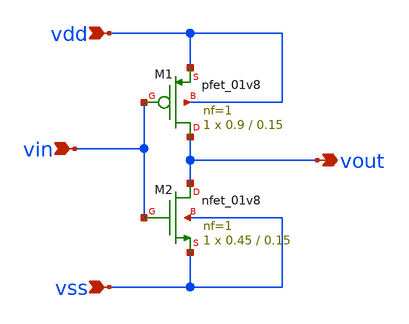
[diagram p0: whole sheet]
** sch_path: track_vlsi/lado/sch/inverter.sch
**.subckt inverter vout vdd vin vss
*.opin vout
*.ipin vdd
*.ipin vin
*.ipin vss
XM1 vout vin vdd vdd sky130_fd_pr__pfet_01v8 L=0.15 W=0.9 nf=1 ad='int((nf+1)/2) * W/nf * 0.29' as='int((nf+2)/2) * W/nf * 0.29'
+ pd='2*int((nf+1)/2) * (W/nf + 0.29)' ps='2*int((nf+2)/2) * (W/nf + 0.29)' nrd='0.29 / W' nrs='0.29 / W'
+ sa=0 sb=0 sd=0 mult=1 m=1
XM2 vout vin vss vss sky130_fd_pr__nfet_01v8 L=0.15 W=0.45 nf=1 ad='int((nf+1)/2) * W/nf * 0.29' as='int((nf+2)/2) * W/nf * 0.29'
+ pd='2*int((nf+1)/2) * (W/nf + 0.29)' ps='2*int((nf+2)/2) * (W/nf + 0.29)' nrd='0.29 / W' nrs='0.29 / W'
+ sa=0 sb=0 sd=0 mult=1 m=1
**.ends
.end
